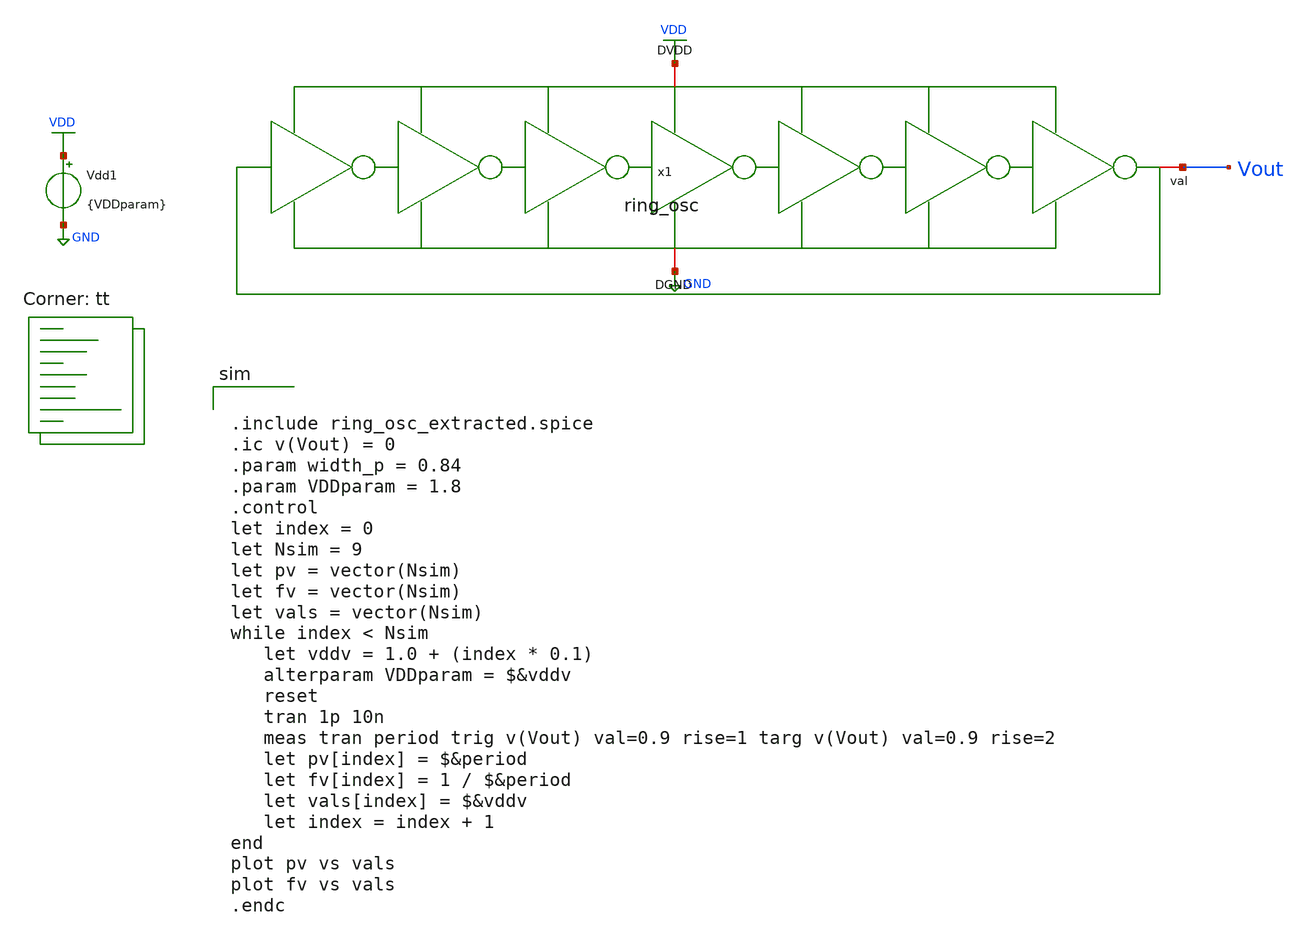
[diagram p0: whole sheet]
** sch_path: tutorial_6/6.2/tutorial_6_2.sch
**.subckt tutorial_6_2
x1 VDD Vout GND ring_osc
Vdd1 VDD GND {VDDparam}
**** begin user architecture code
.lib $::SKYWATER_MODELS/sky130.lib.spice tt


.include ring_osc_extracted.spice
.ic v(Vout) = 0
.param width_p = 0.84
.param VDDparam = 1.8
.control
let index = 0
let Nsim = 9
let pv = vector(Nsim)
let fv = vector(Nsim)
let vals = vector(Nsim)
while index < Nsim
   let vddv = 1.0 + (index * 0.1)
   alterparam VDDparam = $&vddv
   reset
   tran 1p 10n
   meas tran period trig v(Vout) val=0.9 rise=1 targ v(Vout) val=0.9 rise=2
   let pv[index] = $&period
   let fv[index] = 1 / $&period
   let vals[index] = $&vddv
   let index = index + 1
end
plot pv vs vals
plot fv vs vals
.endc

**** end user architecture code
**.ends
.GLOBAL GND
.GLOBAL VDD
.end
